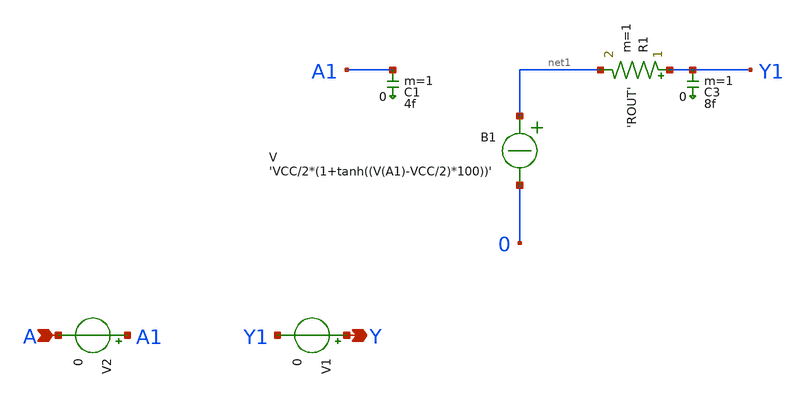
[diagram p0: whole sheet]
** sch_path: xschem_library/ngspice/buf_ngspice.sch
**.subckt buf_ngspice A Y
*.ipin A
*.opin Y
B1 net1 0 V = 'VCC/2*(1+tanh((V(A1)-VCC/2)*100))'
R1 Y1 net1 'ROUT' m=1
C3 Y1 0 8f m=1
C1 A1 0 4f m=1
V1 Y Y1 0
V2 A1 A 0
**.ends
.end
